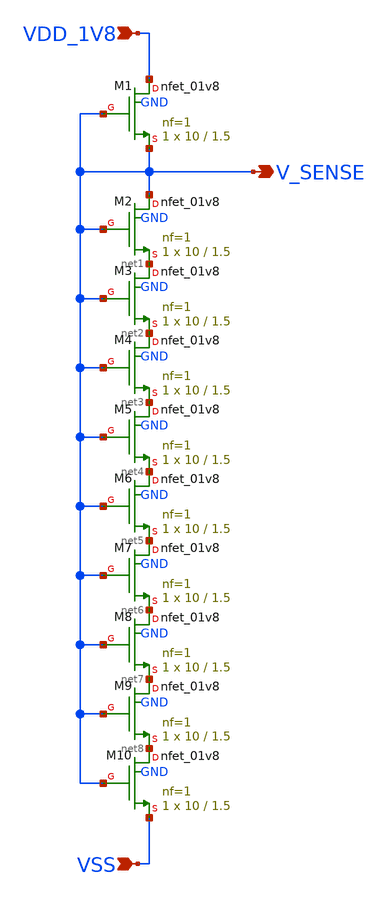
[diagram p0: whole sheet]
** sch_path: design/RPLY_TEMP_SENS_SKY130NM/TEMP_SENS_ELEMENT.sch
**.subckt TEMP_SENS_ELEMENT VDD_1V8 V_SENSE VSS
*.ipin VDD_1V8
*.opin V_SENSE
*.ipin VSS
XM1 VDD_1V8 V_SENSE V_SENSE GND sky130_fd_pr__nfet_01v8 L=1.5 W=10 nf=1 ad='int((nf+1)/2) * W/nf * 0.29'
+ as='int((nf+2)/2) * W/nf * 0.29' pd='2*int((nf+1)/2) * (W/nf + 0.29)' ps='2*int((nf+2)/2) * (W/nf + 0.29)'
+ nrd='0.29 / W' nrs='0.29 / W' sa=0 sb=0 sd=0 mult=1 m=1
XM2 V_SENSE V_SENSE net1 GND sky130_fd_pr__nfet_01v8 L=1.5 W=10 nf=1 ad='int((nf+1)/2) * W/nf * 0.29'
+ as='int((nf+2)/2) * W/nf * 0.29' pd='2*int((nf+1)/2) * (W/nf + 0.29)' ps='2*int((nf+2)/2) * (W/nf + 0.29)'
+ nrd='0.29 / W' nrs='0.29 / W' sa=0 sb=0 sd=0 mult=1 m=1
XM3 net1 V_SENSE net2 GND sky130_fd_pr__nfet_01v8 L=1.5 W=10 nf=1 ad='int((nf+1)/2) * W/nf * 0.29' as='int((nf+2)/2) * W/nf * 0.29'
+ pd='2*int((nf+1)/2) * (W/nf + 0.29)' ps='2*int((nf+2)/2) * (W/nf + 0.29)' nrd='0.29 / W' nrs='0.29 / W'
+ sa=0 sb=0 sd=0 mult=1 m=1
XM4 net2 V_SENSE net3 GND sky130_fd_pr__nfet_01v8 L=1.5 W=10 nf=1 ad='int((nf+1)/2) * W/nf * 0.29' as='int((nf+2)/2) * W/nf * 0.29'
+ pd='2*int((nf+1)/2) * (W/nf + 0.29)' ps='2*int((nf+2)/2) * (W/nf + 0.29)' nrd='0.29 / W' nrs='0.29 / W'
+ sa=0 sb=0 sd=0 mult=1 m=1
XM5 net3 V_SENSE net4 GND sky130_fd_pr__nfet_01v8 L=1.5 W=10 nf=1 ad='int((nf+1)/2) * W/nf * 0.29' as='int((nf+2)/2) * W/nf * 0.29'
+ pd='2*int((nf+1)/2) * (W/nf + 0.29)' ps='2*int((nf+2)/2) * (W/nf + 0.29)' nrd='0.29 / W' nrs='0.29 / W'
+ sa=0 sb=0 sd=0 mult=1 m=1
XM6 net4 V_SENSE net5 GND sky130_fd_pr__nfet_01v8 L=1.5 W=10 nf=1 ad='int((nf+1)/2) * W/nf * 0.29' as='int((nf+2)/2) * W/nf * 0.29'
+ pd='2*int((nf+1)/2) * (W/nf + 0.29)' ps='2*int((nf+2)/2) * (W/nf + 0.29)' nrd='0.29 / W' nrs='0.29 / W'
+ sa=0 sb=0 sd=0 mult=1 m=1
XM7 net5 V_SENSE net6 GND sky130_fd_pr__nfet_01v8 L=1.5 W=10 nf=1 ad='int((nf+1)/2) * W/nf * 0.29' as='int((nf+2)/2) * W/nf * 0.29'
+ pd='2*int((nf+1)/2) * (W/nf + 0.29)' ps='2*int((nf+2)/2) * (W/nf + 0.29)' nrd='0.29 / W' nrs='0.29 / W'
+ sa=0 sb=0 sd=0 mult=1 m=1
XM8 net6 V_SENSE net7 GND sky130_fd_pr__nfet_01v8 L=1.5 W=10 nf=1 ad='int((nf+1)/2) * W/nf * 0.29' as='int((nf+2)/2) * W/nf * 0.29'
+ pd='2*int((nf+1)/2) * (W/nf + 0.29)' ps='2*int((nf+2)/2) * (W/nf + 0.29)' nrd='0.29 / W' nrs='0.29 / W'
+ sa=0 sb=0 sd=0 mult=1 m=1
XM9 net7 V_SENSE net8 GND sky130_fd_pr__nfet_01v8 L=1.5 W=10 nf=1 ad='int((nf+1)/2) * W/nf * 0.29' as='int((nf+2)/2) * W/nf * 0.29'
+ pd='2*int((nf+1)/2) * (W/nf + 0.29)' ps='2*int((nf+2)/2) * (W/nf + 0.29)' nrd='0.29 / W' nrs='0.29 / W'
+ sa=0 sb=0 sd=0 mult=1 m=1
XM10 net8 V_SENSE VSS GND sky130_fd_pr__nfet_01v8 L=1.5 W=10 nf=1 ad='int((nf+1)/2) * W/nf * 0.29' as='int((nf+2)/2) * W/nf * 0.29'
+ pd='2*int((nf+1)/2) * (W/nf + 0.29)' ps='2*int((nf+2)/2) * (W/nf + 0.29)' nrd='0.29 / W' nrs='0.29 / W'
+ sa=0 sb=0 sd=0 mult=1 m=1
**.ends
.end
